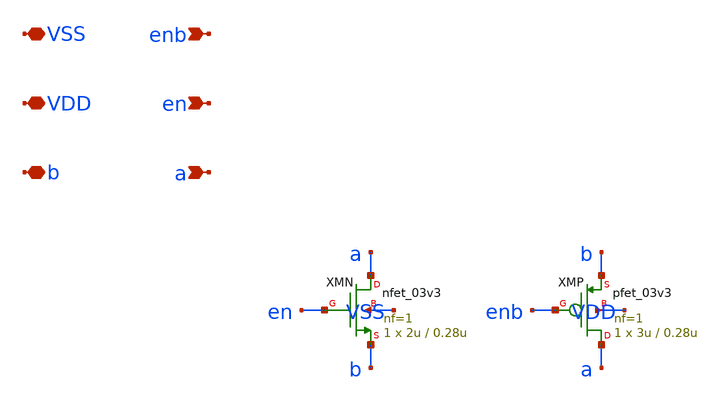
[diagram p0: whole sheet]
** sch_path: design/tg_mux.sch
**.subckt tg_mux a en enb b VDD VSS
*.ipin a
*.ipin en
*.ipin enb
*.iopin b
*.iopin VDD
*.iopin VSS
XMN a en b VSS nfet_03v3 L=0.28u W=2u nf=1 ad='int((nf+1)/2) * W/nf * 0.18u' as='int((nf+2)/2) * W/nf * 0.18u'
+ pd='2*int((nf+1)/2) * (W/nf + 0.18u)' ps='2*int((nf+2)/2) * (W/nf + 0.18u)' nrd='0.18u / W' nrs='0.18u / W'
+ sa=0 sb=0 sd=0 m=1
XMP a enb b VDD pfet_03v3 L=0.28u W=3u nf=1 ad='int((nf+1)/2) * W/nf * 0.18u' as='int((nf+2)/2) * W/nf * 0.18u'
+ pd='2*int((nf+1)/2) * (W/nf + 0.18u)' ps='2*int((nf+2)/2) * (W/nf + 0.18u)' nrd='0.18u / W' nrs='0.18u / W'
+ sa=0 sb=0 sd=0 m=1
**.ends
.end
